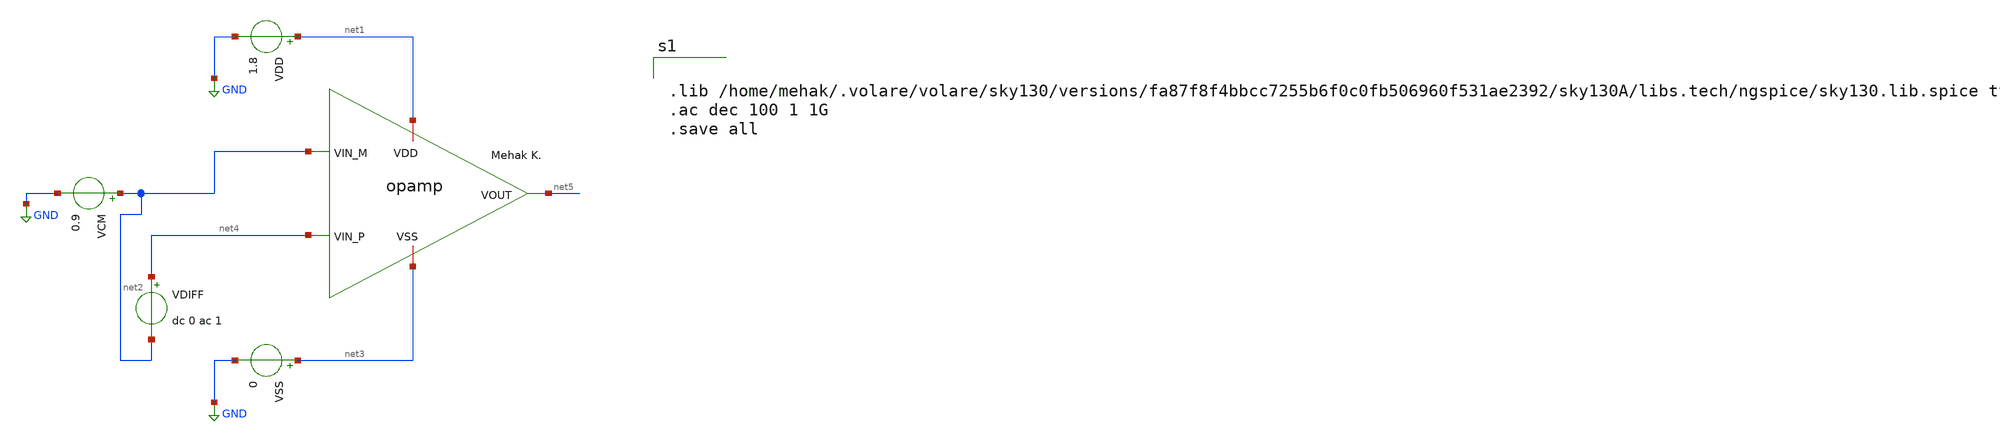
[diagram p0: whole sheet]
** sch_path: analog/build/schematic/tb_ac_analysis.sch
**.subckt tb_ac_analysis
VDD net1 GND 1.8
VSS net3 GND 0
VCM net2 GND 0.9
VDIFF net4 net2 dc 0 ac 1
x1 net1 net5 net2 net4 net3 opamp_two_stage
**** begin user architecture code


.lib /home/mehak/.volare/volare/sky130/versions/fa87f8f4bbcc7255b6f0c0fb506960f531ae2392/sky130A/libs.tech/ngspice/sky130.lib.spice tt
.ac dec 100 1 1G
.save all


**** end user architecture code
**.ends
.GLOBAL GND
.end
